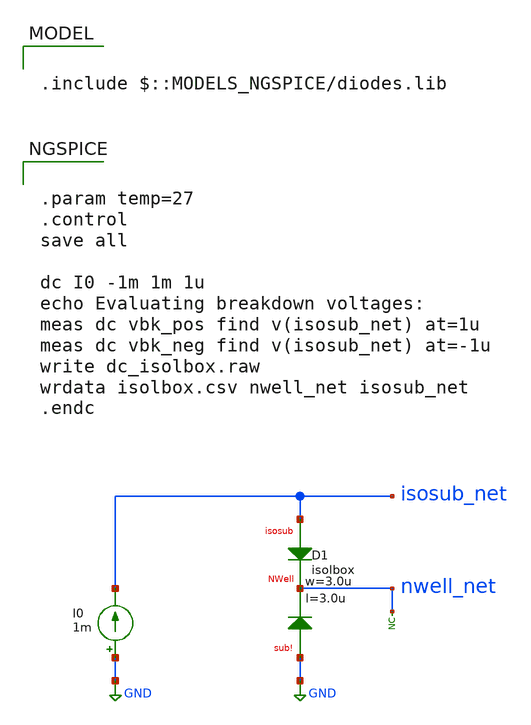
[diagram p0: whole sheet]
** sch_path: ihp-sg13g2/xschem_libs/sg13g2_tests/dc_isolbox/schematic/dc_isolbox.sch
* Copyright 2023 IHP PDK Authors
**.subckt dc_isolbox
I0 GND isosub_net 1m
XD1 isosub_net nwell_net GND isolbox l=3.0u w=3.0u
* noconn nwell_net
**** begin user architecture code

.include $::MODELS_NGSPICE/diodes.lib



.param temp=27
.control
save all

dc I0 -1m 1m 1u
echo Evaluating breakdown voltages:
meas dc vbk_pos find v(isosub_net) at=1u
meas dc vbk_neg find v(isosub_net) at=-1u
write dc_isolbox.raw
wrdata isolbox.csv nwell_net isosub_net
.endc


**** end user architecture code
**.ends
.GLOBAL GND
.end
